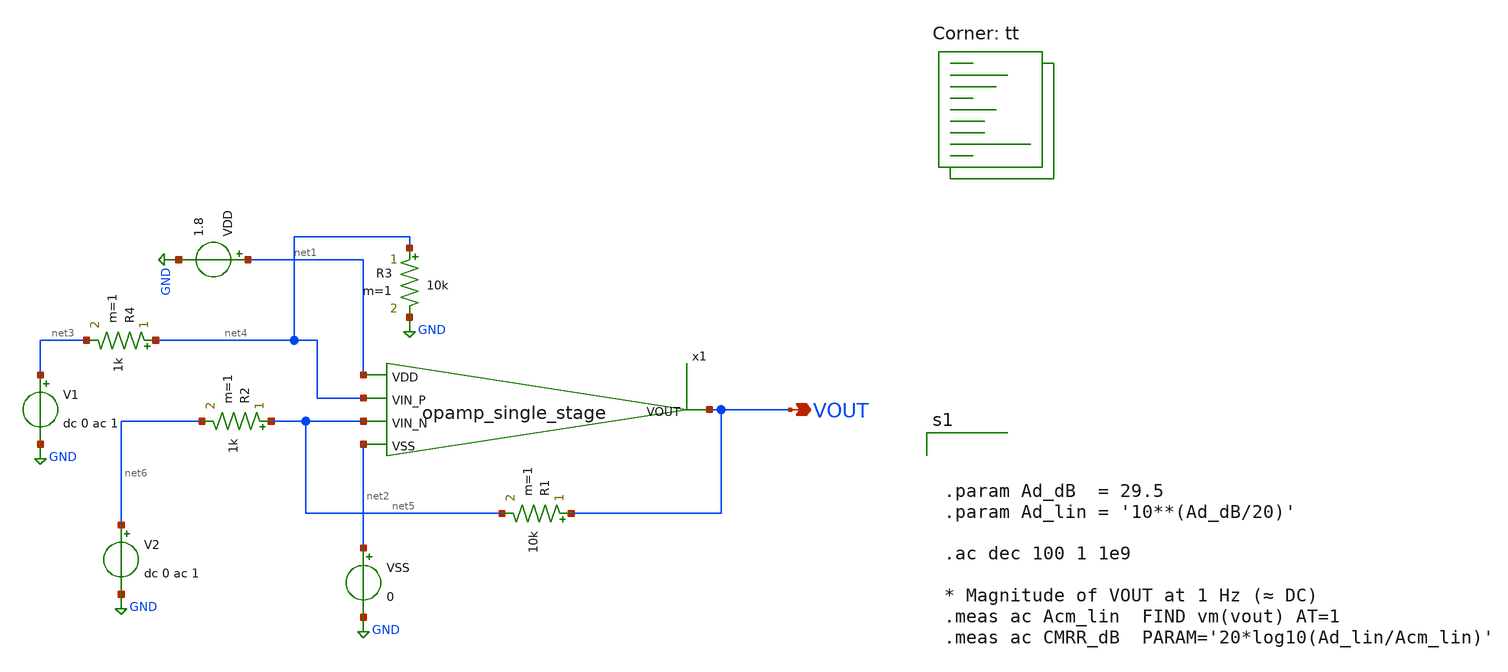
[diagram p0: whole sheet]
** sch_path: analog/schematics/testbenches/tb_cmrr_analysis.sch
**.subckt tb_cmrr_analysis VOUT
*.opin VOUT
x1 net1 VOUT net4 net5 net2 opamp_single_stage
R2 net5 net6 1k m=1
R1 VOUT net5 10k m=1
R3 net4 GND 10k m=1
R4 net4 net3 1k m=1
V1 net3 GND dc 0 ac 1
VDD net1 GND 1.8
VSS net2 GND 0
V2 net6 GND dc 0 ac 1
**** begin user architecture code
.lib $::SKYWATER_MODELS/sky130.lib.spice tt



.param Ad_dB  = 29.5
.param Ad_lin = '10**(Ad_dB/20)'

.ac dec 100 1 1e9

* Magnitude of VOUT at 1 Hz (≈ DC)
.meas ac Acm_lin  FIND vm(vout) AT=1
.meas ac CMRR_dB  PARAM='20*log10(Ad_lin/Acm_lin)'


**** end user architecture code
**.ends

* expanding   symbol:  opamp_single_stage.sym # of pins=5
** sym_path: analog/schematics/opamp_single_stage.sym
** sch_path: analog/schematics/opamp_single_stage.sch
.subckt opamp_single_stage VDD VOUT VIN_P VIN_N VSS
*.ipin VDD
*.ipin VIN_P
*.ipin VIN_N
*.ipin VSS
*.opin VOUT
XM4 net2 net1 VDD VDD sky130_fd_pr__pfet_01v8 L=0.5 W=8 nf=1 ad='int((nf+1)/2) * W/nf * 0.29' as='int((nf+2)/2) * W/nf * 0.29'
+ pd='2*int((nf+1)/2) * (W/nf + 0.29)' ps='2*int((nf+2)/2) * (W/nf + 0.29)' nrd='0.29 / W' nrs='0.29 / W'
+ sa=0 sb=0 sd=0 mult=1 m=1
XM3 net1 net1 VDD VDD sky130_fd_pr__pfet_01v8 L=0.5 W=8 nf=1 ad='int((nf+1)/2) * W/nf * 0.29' as='int((nf+2)/2) * W/nf * 0.29'
+ pd='2*int((nf+1)/2) * (W/nf + 0.29)' ps='2*int((nf+2)/2) * (W/nf + 0.29)' nrd='0.29 / W' nrs='0.29 / W'
+ sa=0 sb=0 sd=0 mult=1 m=1
XM1 net1 VIN_P net3 GND sky130_fd_pr__nfet_01v8_lvt L=0.5 W=6 nf=1 ad='int((nf+1)/2) * W/nf * 0.29' as='int((nf+2)/2) * W/nf * 0.29'
+ pd='2*int((nf+1)/2) * (W/nf + 0.29)' ps='2*int((nf+2)/2) * (W/nf + 0.29)' nrd='0.29 / W' nrs='0.29 / W'
+ sa=0 sb=0 sd=0 mult=1 m=1
XM2 net2 VIN_N net3 GND sky130_fd_pr__nfet_01v8_lvt L=0.5 W=6 nf=1 ad='int((nf+1)/2) * W/nf * 0.29' as='int((nf+2)/2) * W/nf * 0.29'
+ pd='2*int((nf+1)/2) * (W/nf + 0.29)' ps='2*int((nf+2)/2) * (W/nf + 0.29)' nrd='0.29 / W' nrs='0.29 / W'
+ sa=0 sb=0 sd=0 mult=1 m=1
XM5 VOUT net2 VDD VDD sky130_fd_pr__pfet_01v8 L=0.5 W=20 nf=1 ad='int((nf+1)/2) * W/nf * 0.29' as='int((nf+2)/2) * W/nf * 0.29'
+ pd='2*int((nf+1)/2) * (W/nf + 0.29)' ps='2*int((nf+2)/2) * (W/nf + 0.29)' nrd='0.29 / W' nrs='0.29 / W'
+ sa=0 sb=0 sd=0 mult=1 m=1
XC1 net5 VOUT sky130_fd_pr__cap_mim_m3_1 W=25 L=20 MF=1 m=1
XM8 net4 net4 VSS VSS sky130_fd_pr__nfet_01v8_lvt L=1.0 W=2 nf=1 ad='int((nf+1)/2) * W/nf * 0.29' as='int((nf+2)/2) * W/nf * 0.29'
+ pd='2*int((nf+1)/2) * (W/nf + 0.29)' ps='2*int((nf+2)/2) * (W/nf + 0.29)' nrd='0.29 / W' nrs='0.29 / W'
+ sa=0 sb=0 sd=0 mult=1 m=1
XM7 net3 net4 VSS VSS sky130_fd_pr__nfet_01v8_lvt L=1.0 W=4 nf=1 ad='int((nf+1)/2) * W/nf * 0.29' as='int((nf+2)/2) * W/nf * 0.29'
+ pd='2*int((nf+1)/2) * (W/nf + 0.29)' ps='2*int((nf+2)/2) * (W/nf + 0.29)' nrd='0.29 / W' nrs='0.29 / W'
+ sa=0 sb=0 sd=0 mult=1 m=1
XM6 VOUT net4 VSS VSS sky130_fd_pr__nfet_01v8_lvt L=1.0 W=8 nf=1 ad='int((nf+1)/2) * W/nf * 0.29' as='int((nf+2)/2) * W/nf * 0.29'
+ pd='2*int((nf+1)/2) * (W/nf + 0.29)' ps='2*int((nf+2)/2) * (W/nf + 0.29)' nrd='0.29 / W' nrs='0.29 / W'
+ sa=0 sb=0 sd=0 mult=1 m=1
I0 VDD net4 5u
R1 net5 net2 7k m=1
.ends

.GLOBAL GND
.end
